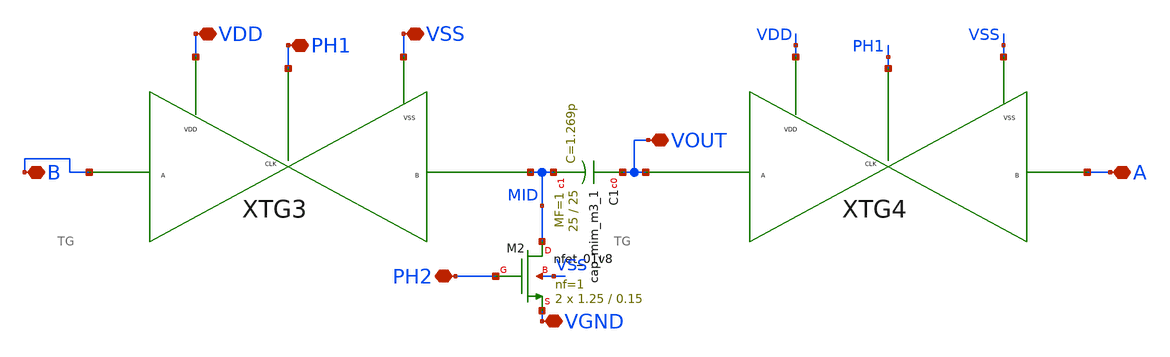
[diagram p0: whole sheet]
** sch_path: xschem/xschem_BGR_Top/Sigma_Delta/Subtractor/Subtractor.sch
**.subckt Subtractor VDD PH1 A VOUT B PH2 VGND VSS
*.iopin VDD
*.iopin PH1
*.iopin A
*.iopin VOUT
*.iopin B
*.iopin PH2
*.iopin VGND
*.iopin VSS
XTG3 VSS PH1 VDD B MID TG
XTG4 VSS PH1 VDD VOUT A TG
XM2 MID PH2 VGND VSS sky130_fd_pr__nfet_01v8 L=0.15 W=1.25 nf=1 ad='int((nf+1)/2) * W/nf * 0.29' as='int((nf+2)/2) * W/nf * 0.29'
+ pd='2*int((nf+1)/2) * (W/nf + 0.29)' ps='2*int((nf+2)/2) * (W/nf + 0.29)' nrd='0.29 / W' nrs='0.29 / W'
+ sa=0 sb=0 sd=0 mult=2 m=2
XC1 VOUT MID sky130_fd_pr__cap_mim_m3_1 W=25 L=25 MF=1 m=1
**** begin user architecture code

** opencircuitdesign pdks install
.lib $::SKYWATER_MODELS/sky130.lib.spice tt


**** end user architecture code
**.ends

* expanding   symbol:  Sigma_Delta/Transmission_Gate/TG.sym # of pins=5
** sym_path: xschem/xschem_BGR_Top/Sigma_Delta/Transmission_Gate/TG.sym
** sch_path: xschem/xschem_BGR_Top/Sigma_Delta/Transmission_Gate/TG.sch
.subckt TG VSS CLK VDD A B
*.iopin VDD
*.iopin VSS
*.iopin A
*.iopin B
*.iopin CLK
XM1 A CLK B VSS sky130_fd_pr__nfet_01v8 L=0.15 W=10 nf=1 ad='int((nf+1)/2) * W/nf * 0.29' as='int((nf+2)/2) * W/nf * 0.29'
+ pd='2*int((nf+1)/2) * (W/nf + 0.29)' ps='2*int((nf+2)/2) * (W/nf + 0.29)' nrd='0.29 / W' nrs='0.29 / W'
+ sa=0 sb=0 sd=0 mult=1 m=1
XM2 B CLKB A VDD sky130_fd_pr__pfet_01v8 L=0.15 W=20 nf=2 ad='int((nf+1)/2) * W/nf * 0.29' as='int((nf+2)/2) * W/nf * 0.29'
+ pd='2*int((nf+1)/2) * (W/nf + 0.29)' ps='2*int((nf+2)/2) * (W/nf + 0.29)' nrd='0.29 / W' nrs='0.29 / W'
+ sa=0 sb=0 sd=0 mult=1 m=1
XM3 CLKB CLK VSS VSS sky130_fd_pr__nfet_01v8 L=0.15 W=10 nf=5 ad='int((nf+1)/2) * W/nf * 0.29' as='int((nf+2)/2) * W/nf * 0.29'
+ pd='2*int((nf+1)/2) * (W/nf + 0.29)' ps='2*int((nf+2)/2) * (W/nf + 0.29)' nrd='0.29 / W' nrs='0.29 / W'
+ sa=0 sb=0 sd=0 mult=1 m=1
XM4 CLKB CLK VDD VDD sky130_fd_pr__pfet_01v8 L=0.15 W=20 nf=10 ad='int((nf+1)/2) * W/nf * 0.29' as='int((nf+2)/2) * W/nf * 0.29'
+ pd='2*int((nf+1)/2) * (W/nf + 0.29)' ps='2*int((nf+2)/2) * (W/nf + 0.29)' nrd='0.29 / W' nrs='0.29 / W'
+ sa=0 sb=0 sd=0 mult=1 m=1
.ends

.end
